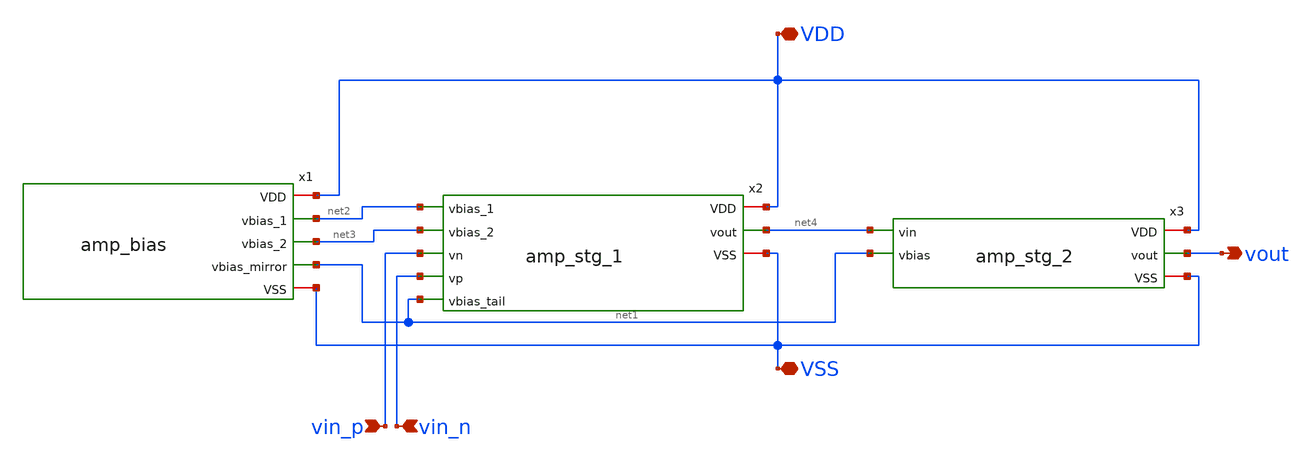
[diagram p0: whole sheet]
** sch_path: xschem/amp_multi_stg.sch
**.subckt amp_multi_stg vout vin_n vin_p VSS VDD
*.opin vout
*.ipin vin_n
*.ipin vin_p
*.iopin VSS
*.iopin VDD
x1 VDD net2 net3 net1 VSS amp_bias
x2 VDD net4 net2 net3 vin_p vin_n net1 VSS amp_stg_1
x3 VDD net4 vout net1 VSS amp_stg_2
**.ends

* expanding   symbol:  ttgf-ece298-analog-op-amp/xschem/amp_bias.sym # of pins=5
** sym_path: xschem/amp_bias.sym
** sch_path: xschem/amp_bias.sch
.subckt amp_bias VDD vbias_1 vbias_2 vbias_mirror VSS
*.iopin VDD
*.iopin VSS
*.opin vbias_1
*.opin vbias_2
*.opin vbias_mirror
R1 VDD vbias_mirror 48.5k m=1
XM1 vbias_mirror vbias_mirror VSS VSS nfet_03v3 L=0.5u W=8u nf=1 ad='int((nf+1)/2) * W/nf * 0.18u' as='int((nf+2)/2) * W/nf * 0.18u'
+ pd='2*int((nf+1)/2) * (W/nf + 0.18u)' ps='2*int((nf+2)/2) * (W/nf + 0.18u)' nrd='0.18u / W' nrs='0.18u / W'
+ sa=0 sb=0 sd=0 m=1 par=1
XM3 net1 vbias_mirror VSS VSS nfet_03v3 L=1.4u W=8u nf=1 ad='int((nf+1)/2) * W/nf * 0.18u' as='int((nf+2)/2) * W/nf * 0.18u'
+ pd='2*int((nf+1)/2) * (W/nf + 0.18u)' ps='2*int((nf+2)/2) * (W/nf + 0.18u)' nrd='0.18u / W' nrs='0.18u / W'
+ sa=0 sb=0 sd=0 m=1 par=1
XM4 net1 net1 VDD VDD pfet_03v3 L=0.5u W=8u nf=1 ad='int((nf+1)/2) * W/nf * 0.18u' as='int((nf+2)/2) * W/nf * 0.18u'
+ pd='2*int((nf+1)/2) * (W/nf + 0.18u)' ps='2*int((nf+2)/2) * (W/nf + 0.18u)' nrd='0.18u / W' nrs='0.18u / W'
+ sa=0 sb=0 sd=0 m=1
XM5 vbias_2 net1 VDD VDD pfet_03v3 L=0.5u W=8u nf=1 ad='int((nf+1)/2) * W/nf * 0.18u' as='int((nf+2)/2) * W/nf * 0.18u'
+ pd='2*int((nf+1)/2) * (W/nf + 0.18u)' ps='2*int((nf+2)/2) * (W/nf + 0.18u)' nrd='0.18u / W' nrs='0.18u / W'
+ sa=0 sb=0 sd=0 m=1
XM6 vbias_1 vbias_mirror VSS VSS nfet_03v3 L=1.4u W=8u nf=1 ad='int((nf+1)/2) * W/nf * 0.18u' as='int((nf+2)/2) * W/nf * 0.18u'
+ pd='2*int((nf+1)/2) * (W/nf + 0.18u)' ps='2*int((nf+2)/2) * (W/nf + 0.18u)' nrd='0.18u / W' nrs='0.18u / W'
+ sa=0 sb=0 sd=0 m=1 par=1
XM7 net2 net2 VSS VSS nfet_03v3 L=0.5u W=14u nf=1 ad='int((nf+1)/2) * W/nf * 0.18u' as='int((nf+2)/2) * W/nf * 0.18u'
+ pd='2*int((nf+1)/2) * (W/nf + 0.18u)' ps='2*int((nf+2)/2) * (W/nf + 0.18u)' nrd='0.18u / W' nrs='0.18u / W'
+ sa=0 sb=0 sd=0 m=1 par=1
XM8 vbias_2 vbias_2 net2 VSS nfet_03v3 L=0.5u W=12u nf=1 ad='int((nf+1)/2) * W/nf * 0.18u' as='int((nf+2)/2) * W/nf * 0.18u'
+ pd='2*int((nf+1)/2) * (W/nf + 0.18u)' ps='2*int((nf+2)/2) * (W/nf + 0.18u)' nrd='0.18u / W' nrs='0.18u / W'
+ sa=0 sb=0 sd=0 m=1 par=1
XM9 vbias_1 vbias_1 VDD VDD pfet_03v3 L=1.4u W=2u nf=1 ad='int((nf+1)/2) * W/nf * 0.18u' as='int((nf+2)/2) * W/nf * 0.18u'
+ pd='2*int((nf+1)/2) * (W/nf + 0.18u)' ps='2*int((nf+2)/2) * (W/nf + 0.18u)' nrd='0.18u / W' nrs='0.18u / W'
+ sa=0 sb=0 sd=0 m=1
.ends


* expanding   symbol:  ttgf-ece298-analog-op-amp/xschem/amp_stg_1.sym # of pins=8
** sym_path: xschem/amp_stg_1.sym
** sch_path: xschem/amp_stg_1.sch
.subckt amp_stg_1 VDD vout vbias_1 vbias_2 vn vp vbias_tail VSS
*.iopin VDD
*.iopin VSS
*.ipin vn
*.ipin vp
*.opin vout
*.ipin vbias_tail
*.ipin vbias_2
*.ipin vbias_1
XM2 net3 vbias_1 net1 VDD pfet_03v3 L=2.0u W=28u nf=4 ad='int((nf+1)/2) * W/nf * 0.18u' as='int((nf+2)/2) * W/nf * 0.18u'
+ pd='2*int((nf+1)/2) * (W/nf + 0.18u)' ps='2*int((nf+2)/2) * (W/nf + 0.18u)' nrd='0.18u / W' nrs='0.18u / W'
+ sa=0 sb=0 sd=0 m=1 par=1
XM1 net4 vn net6 VSS nfet_03v3 L=1.4u W=16u nf=2 ad='int((nf+1)/2) * W/nf * 0.18u' as='int((nf+2)/2) * W/nf * 0.18u'
+ pd='2*int((nf+1)/2) * (W/nf + 0.18u)' ps='2*int((nf+2)/2) * (W/nf + 0.18u)' nrd='0.18u / W' nrs='0.18u / W'
+ sa=0 sb=0 sd=0 m=2 par=2
XM3 net6 vbias_tail VSS VSS nfet_03v3 L=1.4u W=32u nf=4 ad='int((nf+1)/2) * W/nf * 0.18u' as='int((nf+2)/2) * W/nf * 0.18u'
+ pd='2*int((nf+1)/2) * (W/nf + 0.18u)' ps='2*int((nf+2)/2) * (W/nf + 0.18u)' nrd='0.18u / W' nrs='0.18u / W'
+ sa=0 sb=0 sd=0 m=1 par=1
XM4 vout vbias_2 net4 VSS nfet_03v3 L=2.0u W=16u nf=4 ad='int((nf+1)/2) * W/nf * 0.18u' as='int((nf+2)/2) * W/nf * 0.18u'
+ pd='2*int((nf+1)/2) * (W/nf + 0.18u)' ps='2*int((nf+2)/2) * (W/nf + 0.18u)' nrd='0.18u / W' nrs='0.18u / W'
+ sa=0 sb=0 sd=0 m=1 par=1
XM5 net3 vbias_2 net5 VSS nfet_03v3 L=2.0u W=16u nf=4 ad='int((nf+1)/2) * W/nf * 0.18u' as='int((nf+2)/2) * W/nf * 0.18u'
+ pd='2*int((nf+1)/2) * (W/nf + 0.18u)' ps='2*int((nf+2)/2) * (W/nf + 0.18u)' nrd='0.18u / W' nrs='0.18u / W'
+ sa=0 sb=0 sd=0 m=1 par=1
XM7 net5 vp net6 VSS nfet_03v3 L=1.4u W=16u nf=2 ad='int((nf+1)/2) * W/nf * 0.18u' as='int((nf+2)/2) * W/nf * 0.18u'
+ pd='2*int((nf+1)/2) * (W/nf + 0.18u)' ps='2*int((nf+2)/2) * (W/nf + 0.18u)' nrd='0.18u / W' nrs='0.18u / W'
+ sa=0 sb=0 sd=0 m=2 par=2
XM8 vout vbias_1 net2 VDD pfet_03v3 L=2.0u W=28u nf=4 ad='int((nf+1)/2) * W/nf * 0.18u' as='int((nf+2)/2) * W/nf * 0.18u'
+ pd='2*int((nf+1)/2) * (W/nf + 0.18u)' ps='2*int((nf+2)/2) * (W/nf + 0.18u)' nrd='0.18u / W' nrs='0.18u / W'
+ sa=0 sb=0 sd=0 m=1 par=1
XM9 net1 net3 VDD VDD pfet_03v3 L=2.0u W=28u nf=4 ad='int((nf+1)/2) * W/nf * 0.18u' as='int((nf+2)/2) * W/nf * 0.18u'
+ pd='2*int((nf+1)/2) * (W/nf + 0.18u)' ps='2*int((nf+2)/2) * (W/nf + 0.18u)' nrd='0.18u / W' nrs='0.18u / W'
+ sa=0 sb=0 sd=0 m=1 par=1
XM10 net2 net3 VDD VDD pfet_03v3 L=2.0u W=28u nf=4 ad='int((nf+1)/2) * W/nf * 0.18u' as='int((nf+2)/2) * W/nf * 0.18u'
+ pd='2*int((nf+1)/2) * (W/nf + 0.18u)' ps='2*int((nf+2)/2) * (W/nf + 0.18u)' nrd='0.18u / W' nrs='0.18u / W'
+ sa=0 sb=0 sd=0 m=1 par=1
.ends


* expanding   symbol:  ttgf-ece298-analog-op-amp/xschem/amp_stg_2.sym # of pins=5
** sym_path: xschem/amp_stg_2.sym
** sch_path: xschem/amp_stg_2.sch
.subckt amp_stg_2 VDD vin vout vbias VSS
*.ipin vin
*.ipin vbias
*.iopin VSS
*.iopin VDD
*.opin vout
XM1 vout vin VDD VDD pfet_03v3 L=0.5u W=16u nf=1 ad='int((nf+1)/2) * W/nf * 0.18u' as='int((nf+2)/2) * W/nf * 0.18u'
+ pd='2*int((nf+1)/2) * (W/nf + 0.18u)' ps='2*int((nf+2)/2) * (W/nf + 0.18u)' nrd='0.18u / W' nrs='0.18u / W'
+ sa=0 sb=0 sd=0 m=1 par=1
XM5 vout vbias VSS VSS nfet_03v3 L=0.5u W=8.0u nf=1 ad='int((nf+1)/2) * W/nf * 0.18u' as='int((nf+2)/2) * W/nf * 0.18u'
+ pd='2*int((nf+1)/2) * (W/nf + 0.18u)' ps='2*int((nf+2)/2) * (W/nf + 0.18u)' nrd='0.18u / W' nrs='0.18u / W'
+ sa=0 sb=0 sd=0 m=1 par=1
C2 vin net1 3p m=1
R2 net1 vout 4.7k m=1
.ends

.end
